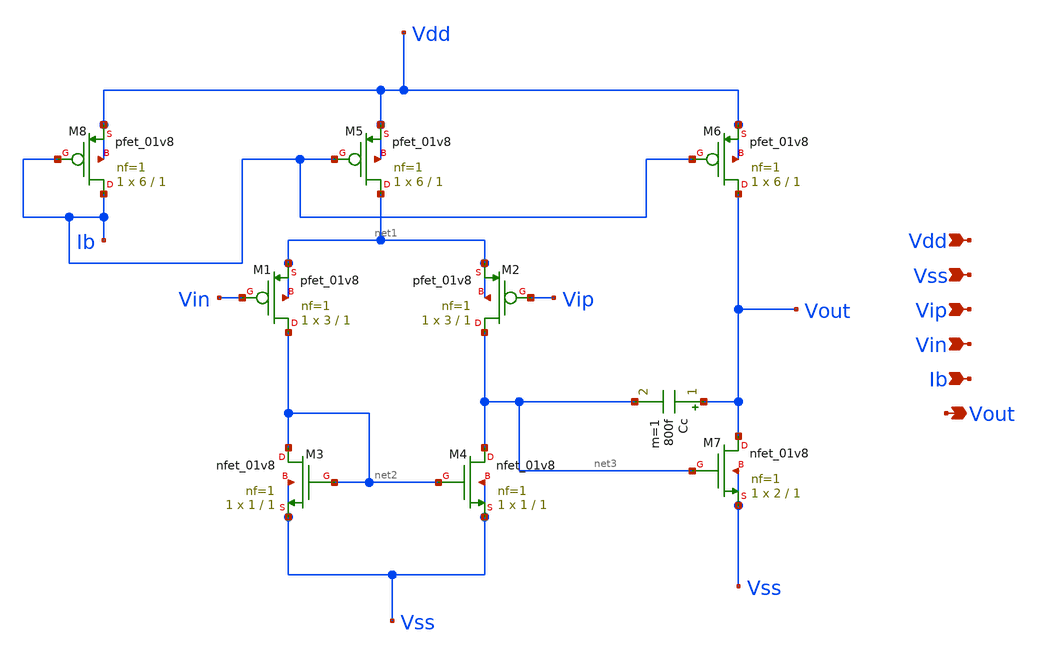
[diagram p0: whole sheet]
** sch_path: temp_sensor_sky130nm/design/TEMP_SENSOR_SKY130NM/OTA.sch
**.subckt OTA Vdd Vss Vip Vin Ib Vout
*.ipin Vdd
*.ipin Vss
*.ipin Vip
*.ipin Vin
*.ipin Ib
*.opin Vout
Cc Vout net3 800f m=1
XM1 net2 Vin net1 net1 sky130_fd_pr__pfet_01v8 L=1 W=3 nf=1 ad='int((nf+1)/2) * W/nf * 0.29' as='int((nf+2)/2) * W/nf * 0.29'
+ pd='2*int((nf+1)/2) * (W/nf + 0.29)' ps='2*int((nf+2)/2) * (W/nf + 0.29)' nrd='0.29 / W' nrs='0.29 / W'
+ sa=0 sb=0 sd=0 mult=1 m=1
XM2 net3 Vip net1 net1 sky130_fd_pr__pfet_01v8 L=1 W=3 nf=1 ad='int((nf+1)/2) * W/nf * 0.29' as='int((nf+2)/2) * W/nf * 0.29'
+ pd='2*int((nf+1)/2) * (W/nf + 0.29)' ps='2*int((nf+2)/2) * (W/nf + 0.29)' nrd='0.29 / W' nrs='0.29 / W'
+ sa=0 sb=0 sd=0 mult=1 m=1
XM3 net2 net2 Vss Vss sky130_fd_pr__nfet_01v8 L=1 W=1 nf=1 ad='int((nf+1)/2) * W/nf * 0.29' as='int((nf+2)/2) * W/nf * 0.29'
+ pd='2*int((nf+1)/2) * (W/nf + 0.29)' ps='2*int((nf+2)/2) * (W/nf + 0.29)' nrd='0.29 / W' nrs='0.29 / W'
+ sa=0 sb=0 sd=0 mult=1 m=1
XM4 net3 net2 Vss Vss sky130_fd_pr__nfet_01v8 L=1 W=1 nf=1 ad='int((nf+1)/2) * W/nf * 0.29' as='int((nf+2)/2) * W/nf * 0.29'
+ pd='2*int((nf+1)/2) * (W/nf + 0.29)' ps='2*int((nf+2)/2) * (W/nf + 0.29)' nrd='0.29 / W' nrs='0.29 / W'
+ sa=0 sb=0 sd=0 mult=1 m=1
XM5 net1 Ib Vdd Vdd sky130_fd_pr__pfet_01v8 L=1 W=6 nf=1 ad='int((nf+1)/2) * W/nf * 0.29' as='int((nf+2)/2) * W/nf * 0.29'
+ pd='2*int((nf+1)/2) * (W/nf + 0.29)' ps='2*int((nf+2)/2) * (W/nf + 0.29)' nrd='0.29 / W' nrs='0.29 / W'
+ sa=0 sb=0 sd=0 mult=1 m=1
XM6 Vout Ib Vdd Vdd sky130_fd_pr__pfet_01v8 L=1 W=6 nf=1 ad='int((nf+1)/2) * W/nf * 0.29' as='int((nf+2)/2) * W/nf * 0.29'
+ pd='2*int((nf+1)/2) * (W/nf + 0.29)' ps='2*int((nf+2)/2) * (W/nf + 0.29)' nrd='0.29 / W' nrs='0.29 / W'
+ sa=0 sb=0 sd=0 mult=1 m=1
XM7 Vout net3 Vss Vss sky130_fd_pr__nfet_01v8 L=1 W=2 nf=1 ad='int((nf+1)/2) * W/nf * 0.29' as='int((nf+2)/2) * W/nf * 0.29'
+ pd='2*int((nf+1)/2) * (W/nf + 0.29)' ps='2*int((nf+2)/2) * (W/nf + 0.29)' nrd='0.29 / W' nrs='0.29 / W'
+ sa=0 sb=0 sd=0 mult=1 m=1
XM8 Ib Ib Vdd Vdd sky130_fd_pr__pfet_01v8 L=1 W=6 nf=1 ad='int((nf+1)/2) * W/nf * 0.29' as='int((nf+2)/2) * W/nf * 0.29'
+ pd='2*int((nf+1)/2) * (W/nf + 0.29)' ps='2*int((nf+2)/2) * (W/nf + 0.29)' nrd='0.29 / W' nrs='0.29 / W'
+ sa=0 sb=0 sd=0 mult=1 m=1
**.ends
.end
